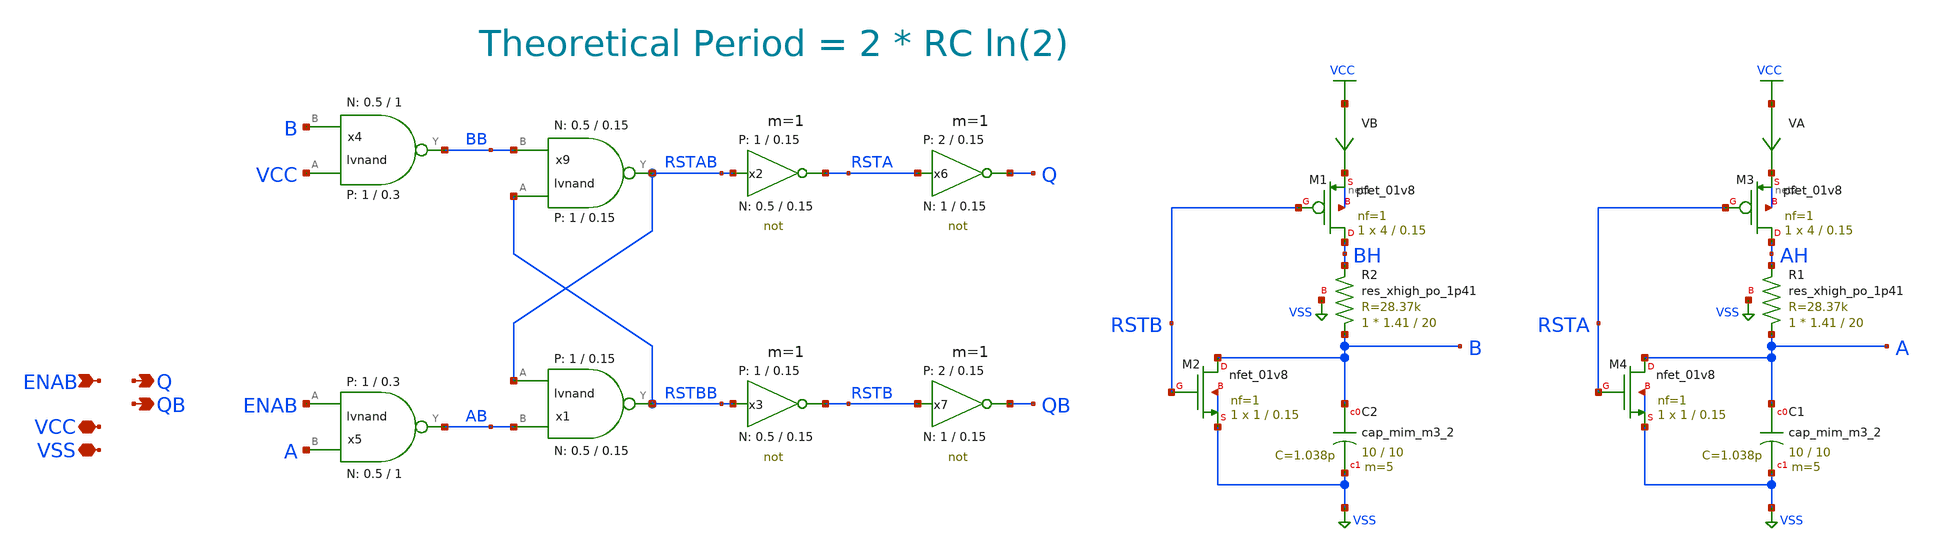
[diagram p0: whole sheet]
** sch_path: sky130A/xschem_libs/sky130_tests_ase/sky130_oscillator/schematic/sky130_oscillator.sch
**.subckt sky130_oscillator VSS VCC ENAB QB Q
*.iopin VSS
*.iopin VCC
*.ipin ENAB
*.opin QB
*.opin Q
x9 RSTBB BB RSTAB VCC VSS lvnand WidthN=0.5 LenN=0.15 WidthP=1 LenP=0.15 m=1
x1 RSTAB AB RSTBB VCC VSS lvnand WidthN=0.5 LenN=0.15 WidthP=1 LenP=0.15 m=1
XM1 BH RSTB net1 net1 sky130_fd_pr__pfet_01v8 L=0.15 W=4 nf=1 ad='int((nf+1)/2) * W/nf * 0.29' as='int((nf+2)/2) * W/nf * 0.29'
+ pd='2*int((nf+1)/2) * (W/nf + 0.29)' ps='2*int((nf+2)/2) * (W/nf + 0.29)' nrd='0.29 / W' nrs='0.29 / W'
+ sa=0 sb=0 sd=0 mult=1 m=1
XM2 B RSTB VSS VSS sky130_fd_pr__nfet_01v8 L=0.15 W=1 nf=1 ad='int((1 + 1)/2) * 1 / 1 * 0.29' as='int((1 + 2)/2) * 1 / 1 * 0.29'
+ pd='2*int((1 + 1)/2) * (1 / 1 + 0.29)' ps='2*int((1 + 2)/2) * (1 / 1 + 0.29)' nrd='0.29 / 1 ' nrs='0.29 / 1 '
+ sa=0 sb=0 sd=0 mult=1 m=1
x2 RSTA RSTAB VCC VSS not W_N=0.5 L_N=0.15 W_P=1 L_P=0.15 m=1
x3 RSTB RSTBB VCC VSS not W_N=0.5 L_N=0.15 W_P=1 L_P=0.15 m=1
x4 VCC B BB VCC VSS lvnand WidthN=0.5 LenN=1 WidthP=1 LenP=0.3 m=1
x5 ENAB A AB VCC VSS lvnand WidthN=0.5 LenN=1 WidthP=1 LenP=0.3 m=1
XM3 AH RSTA net2 net2 sky130_fd_pr__pfet_01v8 L=0.15 W=4 nf=1 ad='int((nf+1)/2) * W/nf * 0.29' as='int((nf+2)/2) * W/nf * 0.29'
+ pd='2*int((nf+1)/2) * (W/nf + 0.29)' ps='2*int((nf+2)/2) * (W/nf + 0.29)' nrd='0.29 / W' nrs='0.29 / W'
+ sa=0 sb=0 sd=0 mult=1 m=1
XM4 A RSTA VSS VSS sky130_fd_pr__nfet_01v8 L=0.15 W=1 nf=1 ad='int((1 + 1)/2) * 1 / 1 * 0.29' as='int((1 + 2)/2) * 1 / 1 * 0.29'
+ pd='2*int((1 + 1)/2) * (1 / 1 + 0.29)' ps='2*int((1 + 2)/2) * (1 / 1 + 0.29)' nrd='0.29 / 1 ' nrs='0.29 / 1 '
+ sa=0 sb=0 sd=0 mult=1 m=1
x6 Q RSTA VCC VSS not W_N=1 L_N=0.15 W_P=2 L_P=0.15 m=1
x7 QB RSTB VCC VSS not W_N=1 L_N=0.15 W_P=2 L_P=0.15 m=1
XC2 B VSS sky130_fd_pr__cap_mim_m3_2 W=10 L=10 MF=5 m=5
XC1 A VSS sky130_fd_pr__cap_mim_m3_2 W=10 L=10 MF=5 m=5
XR1 A AH VSS sky130_fd_pr__res_xhigh_po_1p41 L=20 mult=1 m=1
XR2 B BH VSS sky130_fd_pr__res_xhigh_po_1p41 L=20 mult=1 m=1
VB VCC net1 0
VA VCC net2 0
**** begin user architecture code


vvcc vcc 0 'VCC'
vvss vss 0 0
venab enab 0 pwl 0 0 100n 0 101n 'VCC'500n 'VCC' 501n 0


**** end user architecture code
**.ends
.GLOBAL VCC
.GLOBAL VSS
.end
